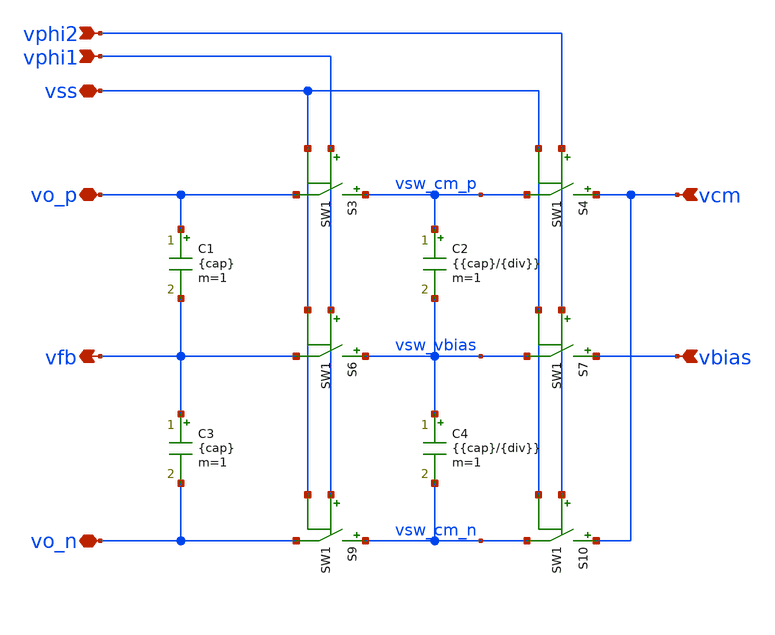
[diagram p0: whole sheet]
** sch_path: xschem/cmfb_sc.sch
**.subckt cmfb_sc vcm vphi2 vphi1 vss vbias vo_p vo_n vfb
*.ipin vcm
*.ipin vphi2
*.ipin vphi1
*.iopin vss
*.ipin vbias
*.iopin vo_p
*.iopin vo_n
*.opin vfb
C1 vo_p vfb {cap} m=1
C2 vsw_cm_p vsw_vbias {{cap}/{div}} m=1
C3 vfb vo_n {cap} m=1
C4 vsw_vbias vsw_cm_n {{cap}/{div}} m=1
S3 vsw_cm_p vo_p vphi1 vss SW1
S4 vcm vsw_cm_p vphi2 vss SW1
S6 vsw_vbias vfb vphi1 vss SW1
S7 vbias vsw_vbias vphi2 vss SW1
S9 vsw_cm_n vo_n vphi1 vss SW1
S10 vcm vsw_cm_n vphi2 vss SW1
**.ends
**** begin user architecture code
.MODEL SW1 SW( VT=0.75 VH=0.01 RON=1 ROFF=1G )
**** end user architecture code
.end
